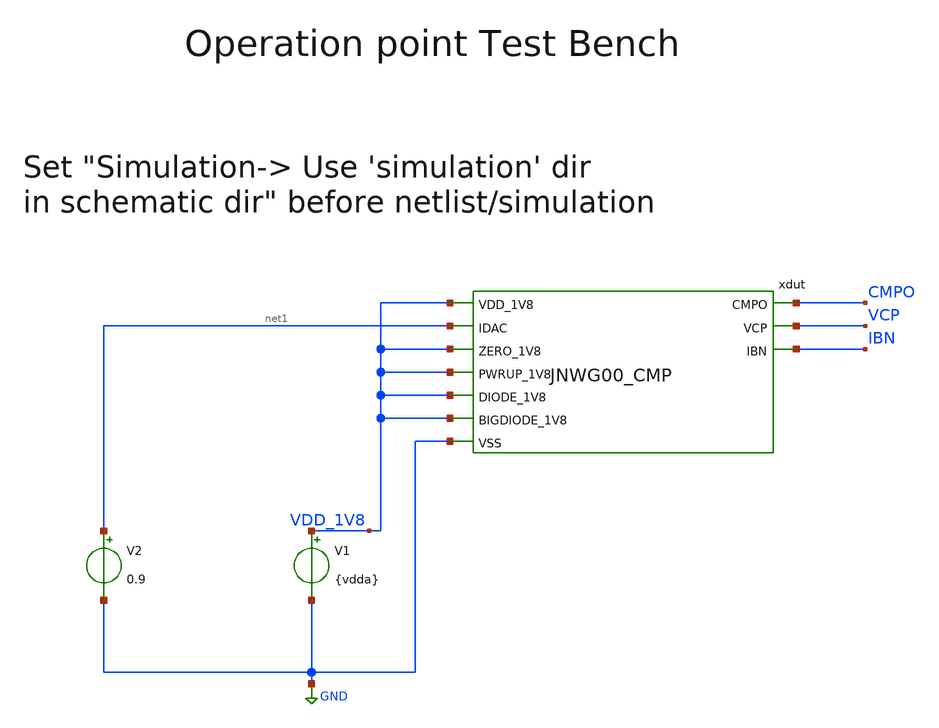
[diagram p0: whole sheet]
** sch_path: design/JNW_GR00_SKY130NM/TB_CMP.sch
**.subckt TB_CMP
V1 VDD_1V8 GND {vdda}
V2 net1 GND 0.9
xdut VDD_1V8 CMPO net1 VDD_1V8 VDD_1V8 VDD_1V8 VCP IBN VDD_1V8 GND JNWG00_CMP
**** begin user architecture code



* ngspice commands
.include corner.spi



**** end user architecture code
**.ends
.GLOBAL GND
.end
